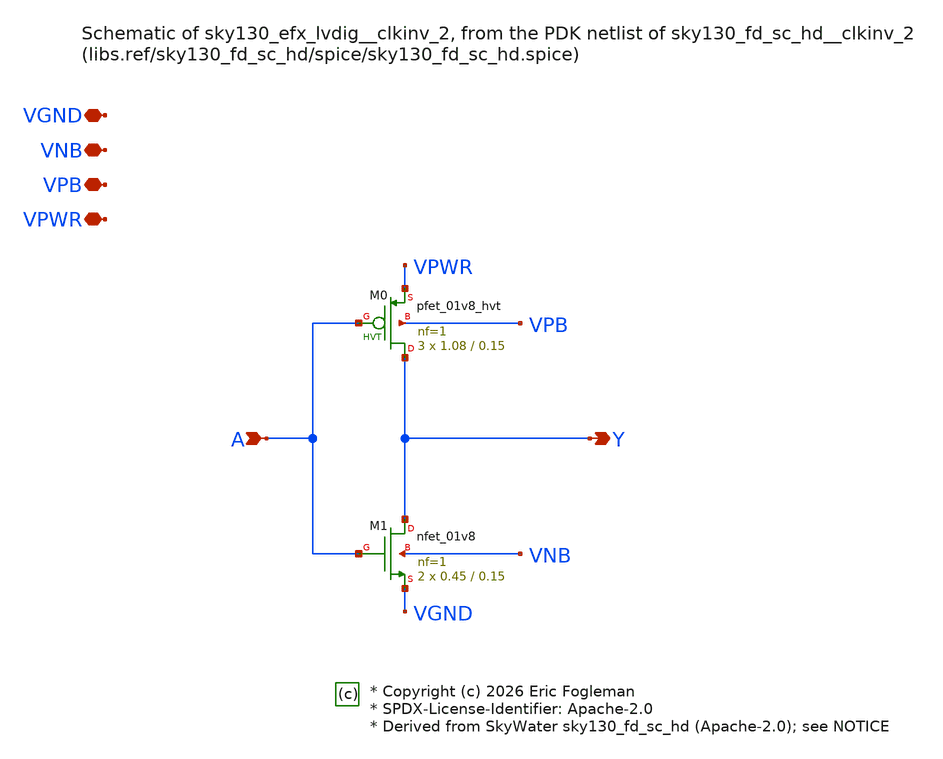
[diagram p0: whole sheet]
** sch_path: xschem/sky130_efx_lvdig__clkinv_2.sch

* Copyright (c) 2026 Eric Fogleman
* SPDX-License-Identifier: Apache-2.0
* Derived from SkyWater sky130_fd_sc_hd (Apache-2.0); see NOTICE

**.subckt sky130_efx_lvdig__clkinv_2 A Y VGND VNB VPB VPWR
*.ipin A
*.opin Y
*.iopin VGND
*.iopin VNB
*.iopin VPB
*.iopin VPWR
XM0 Y A VPWR VPB sky130_fd_pr__pfet_01v8_hvt L=0.15 W=1.08 nf=1 ad='int((1 + 1)/2) * 1.08 / 1 * 0.29'
+ as='int((1 + 2)/2) * 1.08 / 1 * 0.29' pd='2*int((1 + 1)/2) * (1.08 / 1 + 0.29)' ps='2*int((1 + 2)/2) * (1.08 / 1 + 0.29)'
+ nrd='0.29 / 1.08 ' nrs='0.29 / 1.08 ' sa=0 sb=0 sd=0 mult=3 m=3
XM1 Y A VGND VNB sky130_fd_pr__nfet_01v8 L=0.15 W=0.45 nf=1 ad='int((1 + 1)/2) * 0.45 / 1 * 0.29' as='int((1 + 2)/2) * 0.45 / 1 * 0.29'
+ pd='2*int((1 + 1)/2) * (0.45 / 1 + 0.29)' ps='2*int((1 + 2)/2) * (0.45 / 1 + 0.29)' nrd='0.29 / 0.45 '
+ nrs='0.29 / 0.45 ' sa=0 sb=0 sd=0 mult=2 m=2
**.ends
.end
